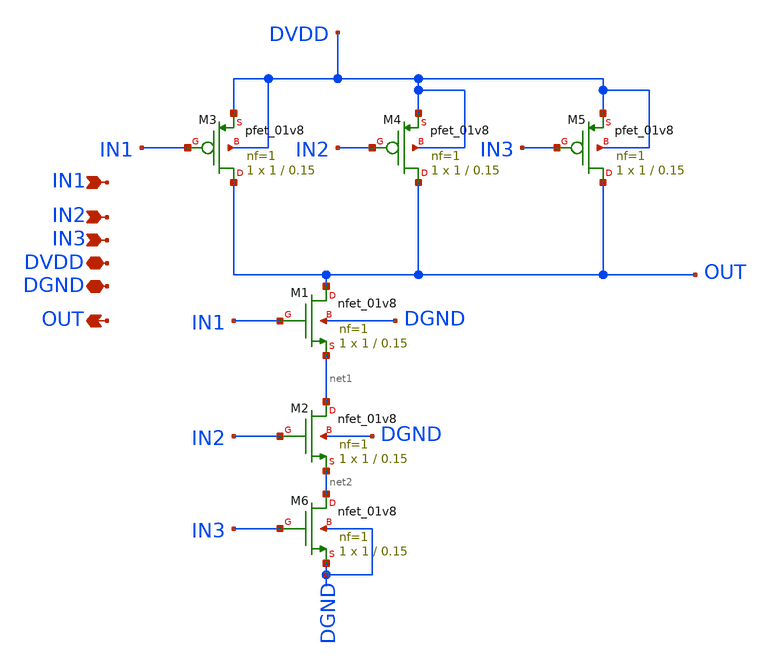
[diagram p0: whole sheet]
** sch_path: NAND3_eymenunay.sch
**.subckt NAND3_eymenunay IN1 IN2 OUT DVDD DGND IN3
*.ipin IN1
*.ipin IN2
*.opin OUT
*.iopin DVDD
*.iopin DGND
*.ipin IN3
XM1 OUT IN1 net1 DGND sky130_fd_pr__nfet_01v8 L=0.15 W=1 nf=1 ad='int((nf+1)/2) * W/nf * 0.29' as='int((nf+2)/2) * W/nf * 0.29'
+ pd='2*int((nf+1)/2) * (W/nf + 0.29)' ps='2*int((nf+2)/2) * (W/nf + 0.29)' nrd='0.29 / W' nrs='0.29 / W'
+ sa=0 sb=0 sd=0 mult=1 m=1
XM2 net1 IN2 net2 DGND sky130_fd_pr__nfet_01v8 L=0.15 W=1 nf=1 ad='int((nf+1)/2) * W/nf * 0.29' as='int((nf+2)/2) * W/nf * 0.29'
+ pd='2*int((nf+1)/2) * (W/nf + 0.29)' ps='2*int((nf+2)/2) * (W/nf + 0.29)' nrd='0.29 / W' nrs='0.29 / W'
+ sa=0 sb=0 sd=0 mult=1 m=1
XM3 OUT IN1 DVDD DVDD sky130_fd_pr__pfet_01v8 L=0.15 W=1 nf=1 ad='int((nf+1)/2) * W/nf * 0.29' as='int((nf+2)/2) * W/nf * 0.29'
+ pd='2*int((nf+1)/2) * (W/nf + 0.29)' ps='2*int((nf+2)/2) * (W/nf + 0.29)' nrd='0.29 / W' nrs='0.29 / W'
+ sa=0 sb=0 sd=0 mult=1 m=1
XM4 OUT IN2 DVDD DVDD sky130_fd_pr__pfet_01v8 L=0.15 W=1 nf=1 ad='int((nf+1)/2) * W/nf * 0.29' as='int((nf+2)/2) * W/nf * 0.29'
+ pd='2*int((nf+1)/2) * (W/nf + 0.29)' ps='2*int((nf+2)/2) * (W/nf + 0.29)' nrd='0.29 / W' nrs='0.29 / W'
+ sa=0 sb=0 sd=0 mult=1 m=1
XM5 OUT IN3 DVDD DVDD sky130_fd_pr__pfet_01v8 L=0.15 W=1 nf=1 ad='int((nf+1)/2) * W/nf * 0.29' as='int((nf+2)/2) * W/nf * 0.29'
+ pd='2*int((nf+1)/2) * (W/nf + 0.29)' ps='2*int((nf+2)/2) * (W/nf + 0.29)' nrd='0.29 / W' nrs='0.29 / W'
+ sa=0 sb=0 sd=0 mult=1 m=1
XM6 net2 IN3 DGND DGND sky130_fd_pr__nfet_01v8 L=0.15 W=1 nf=1 ad='int((nf+1)/2) * W/nf * 0.29' as='int((nf+2)/2) * W/nf * 0.29'
+ pd='2*int((nf+1)/2) * (W/nf + 0.29)' ps='2*int((nf+2)/2) * (W/nf + 0.29)' nrd='0.29 / W' nrs='0.29 / W'
+ sa=0 sb=0 sd=0 mult=1 m=1
**.ends
.end
